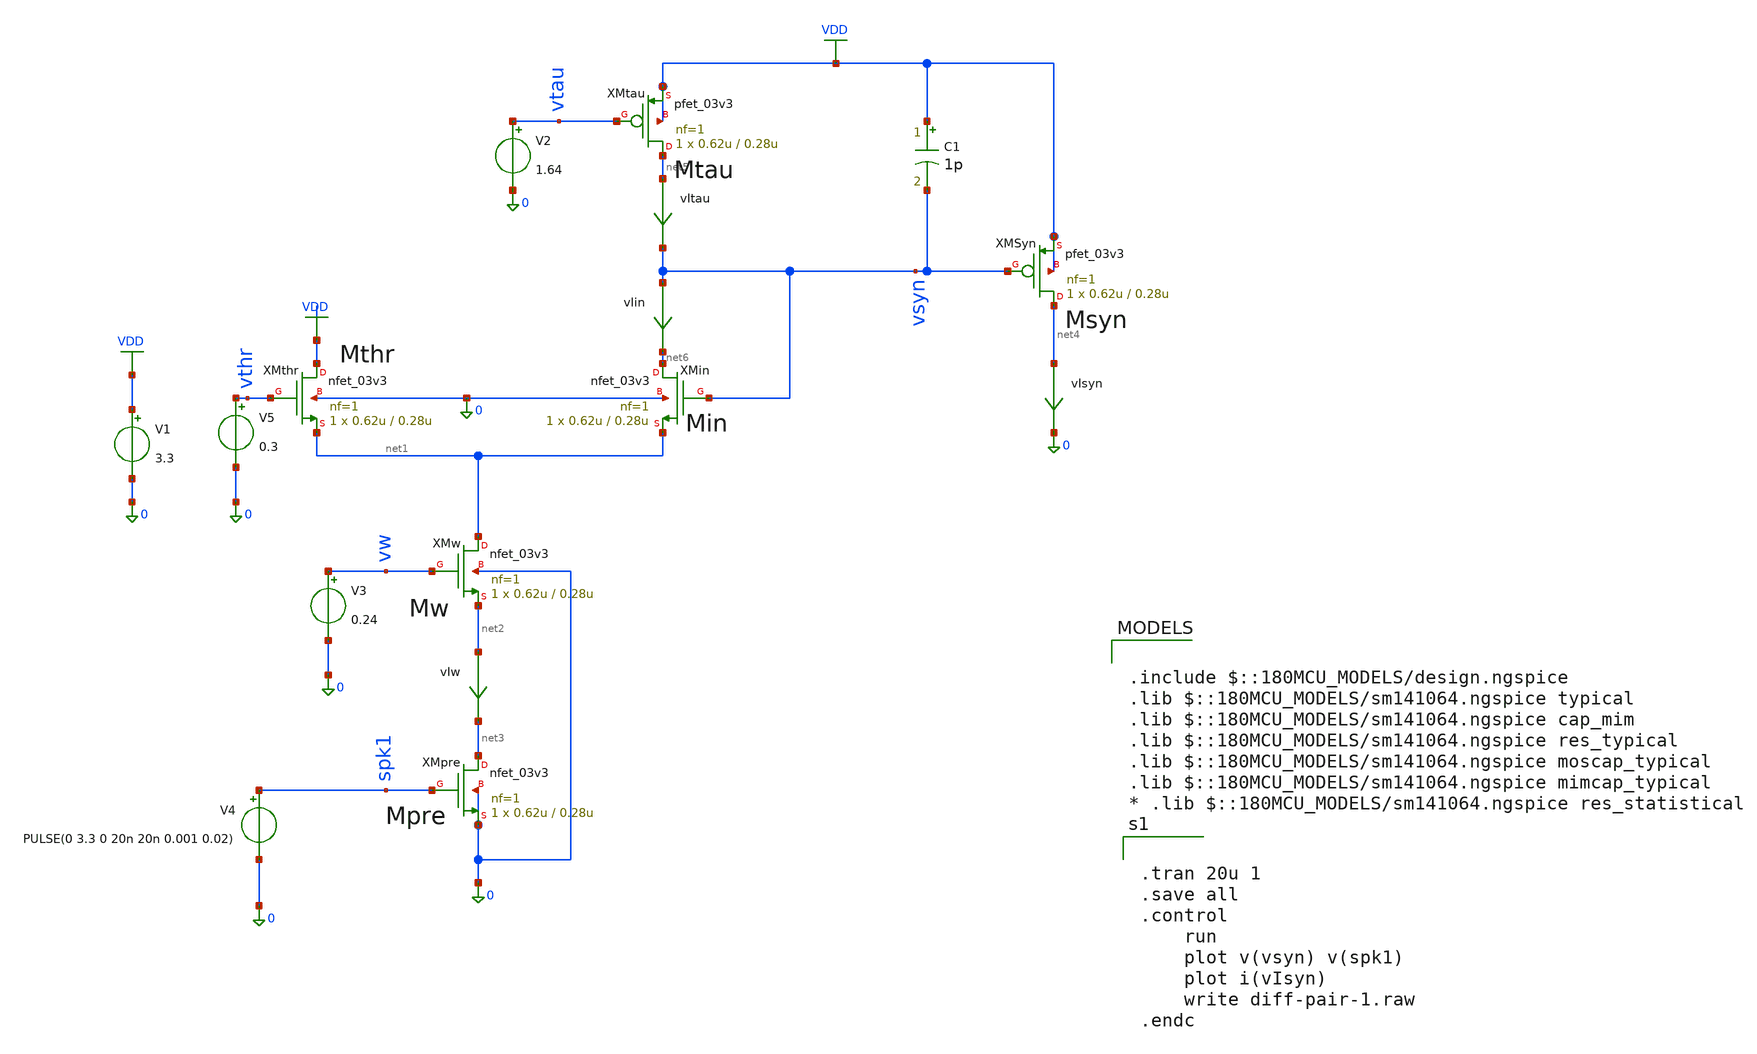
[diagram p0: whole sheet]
** sch_path: sch/integrator/dif-pair-1.sch
**.subckt dif-pair-1
XMtau net5 vtau VDD VDD pfet_03v3 L=0.28u W=0.62u nf=1 ad='int((nf+1)/2) * W/nf * 0.18u' as='int((nf+2)/2) * W/nf * 0.18u'
+ pd='2*int((nf+1)/2) * (W/nf + 0.18u)' ps='2*int((nf+2)/2) * (W/nf + 0.18u)' nrd='0.18u / W' nrs='0.18u / W'
+ sa=0 sb=0 sd=0 m=1
V1 VDD 0 3.3
C1 VDD vsyn 1p m=1
V2 vtau 0 1.64
V3 vw 0 0.24
V4 spk1 0 PULSE(0 3.3 0 20n 20n 0.001 0.02)
XMthr VDD vthr net1 0 nfet_03v3 L=0.28u W=0.62u nf=1 ad='int((nf+1)/2) * W/nf * 0.18u' as='int((nf+2)/2) * W/nf * 0.18u'
+ pd='2*int((nf+1)/2) * (W/nf + 0.18u)' ps='2*int((nf+2)/2) * (W/nf + 0.18u)' nrd='0.18u / W' nrs='0.18u / W'
+ sa=0 sb=0 sd=0 m=1
XMin net6 vsyn net1 0 nfet_03v3 L=0.28u W=0.62u nf=1 ad='int((nf+1)/2) * W/nf * 0.18u' as='int((nf+2)/2) * W/nf * 0.18u'
+ pd='2*int((nf+1)/2) * (W/nf + 0.18u)' ps='2*int((nf+2)/2) * (W/nf + 0.18u)' nrd='0.18u / W' nrs='0.18u / W'
+ sa=0 sb=0 sd=0 m=1
V5 vthr 0 0.3
XMSyn net4 vsyn VDD VDD pfet_03v3 L=0.28u W=0.62u nf=1 ad='int((nf+1)/2) * W/nf * 0.18u' as='int((nf+2)/2) * W/nf * 0.18u'
+ pd='2*int((nf+1)/2) * (W/nf + 0.18u)' ps='2*int((nf+2)/2) * (W/nf + 0.18u)' nrd='0.18u / W' nrs='0.18u / W'
+ sa=0 sb=0 sd=0 m=1
XMw net1 vw net2 0 nfet_03v3 L=0.28u W=0.62u nf=1 ad='int((nf+1)/2) * W/nf * 0.18u' as='int((nf+2)/2) * W/nf * 0.18u'
+ pd='2*int((nf+1)/2) * (W/nf + 0.18u)' ps='2*int((nf+2)/2) * (W/nf + 0.18u)' nrd='0.18u / W' nrs='0.18u / W'
+ sa=0 sb=0 sd=0 m=1
XMpre net3 spk1 0 0 nfet_03v3 L=0.28u W=0.62u nf=1 ad='int((nf+1)/2) * W/nf * 0.18u' as='int((nf+2)/2) * W/nf * 0.18u'
+ pd='2*int((nf+1)/2) * (W/nf + 0.18u)' ps='2*int((nf+2)/2) * (W/nf + 0.18u)' nrd='0.18u / W' nrs='0.18u / W'
+ sa=0 sb=0 sd=0 m=1
vIsyn net4 0 0
.save i(visyn)
vItau net5 vsyn 0
.save i(vitau)
vIin vsyn net6 0
.save i(viin)
vIw net2 net3 0
.save i(viw)
**** begin user architecture code


.tran 20u 1
.save all
.control
	run
	plot v(vsyn) v(spk1)
	plot i(vIsyn)
	write diff-pair-1.raw
.endc




.include $::180MCU_MODELS/design.ngspice
.lib $::180MCU_MODELS/sm141064.ngspice typical
.lib $::180MCU_MODELS/sm141064.ngspice cap_mim
.lib $::180MCU_MODELS/sm141064.ngspice res_typical
.lib $::180MCU_MODELS/sm141064.ngspice moscap_typical
.lib $::180MCU_MODELS/sm141064.ngspice mimcap_typical
* .lib $::180MCU_MODELS/sm141064.ngspice res_statistical

**** end user architecture code
**.ends
.GLOBAL VDD
.end
